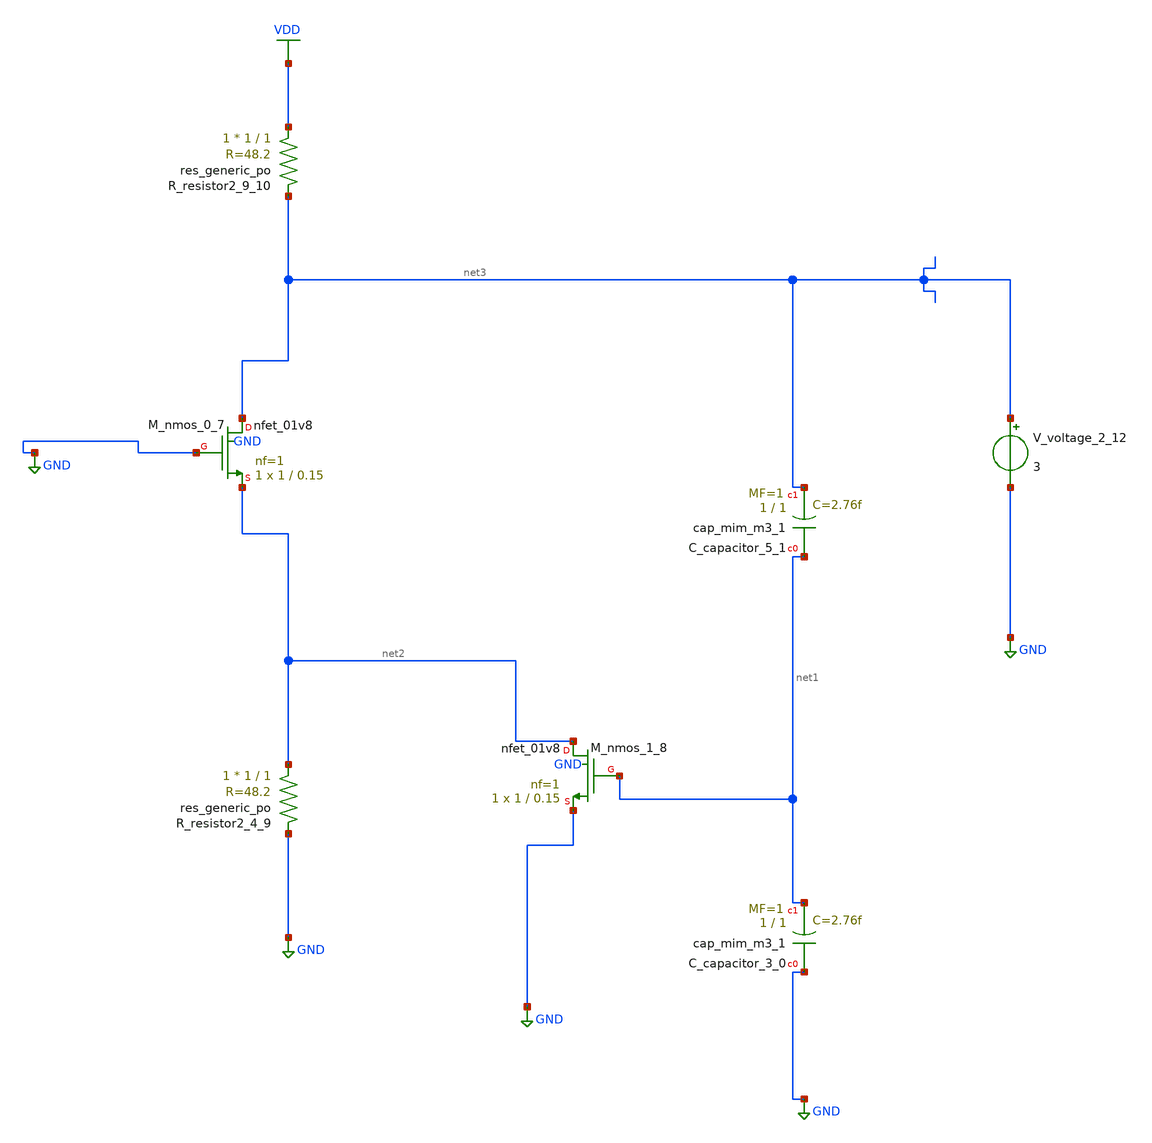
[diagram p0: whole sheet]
** sch_path: schematics/AMSNet/545.sch
**.subckt 545
XC_capacitor_3_0 GND net1 sky130_fd_pr__cap_mim_m3_1 W=1 L=1 MF=1 m=1
XC_capacitor_5_1 net1 net3 sky130_fd_pr__cap_mim_m3_1 W=1 L=1 MF=1 m=1
XM_nmos_0_7 net3 GND net2 GND sky130_fd_pr__nfet_01v8 L=0.15 W=1 nf=1 ad='int((1 + 1)/2) * 1 / 1 * 0.29'
+ as='int((1 + 2)/2) * 1 / 1 * 0.29' pd='2*int((1 + 1)/2) * (1 / 1 + 0.29)' ps='2*int((1 + 2)/2) * (1 / 1 + 0.29)'
+ nrd='0.29 / 1 ' nrs='0.29 / 1 ' sa=0 sb=0 sd=0 mult=1 m=1
XM_nmos_1_8 net2 net1 GND GND sky130_fd_pr__nfet_01v8 L=0.15 W=1 nf=1 ad='int((1 + 1)/2) * 1 / 1 * 0.29'
+ as='int((1 + 2)/2) * 1 / 1 * 0.29' pd='2*int((1 + 1)/2) * (1 / 1 + 0.29)' ps='2*int((1 + 2)/2) * (1 / 1 + 0.29)'
+ nrd='0.29 / 1 ' nrs='0.29 / 1 ' sa=0 sb=0 sd=0 mult=1 m=1
XR_resistor2_4_9 net2 GND sky130_fd_pr__res_generic_po W=1 L=1 m=1
XR_resistor2_9_10 VDD net3 sky130_fd_pr__res_generic_po W=1 L=1 m=1
V_voltage_2_12 net3 GND 3
**.ends
.GLOBAL GND
.GLOBAL VDD
.end
